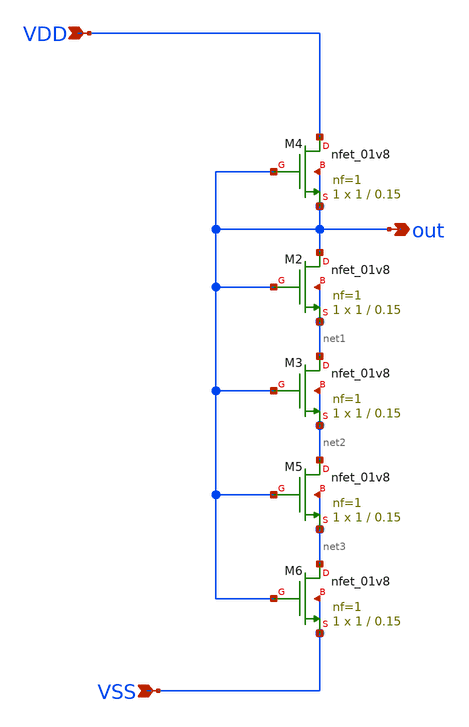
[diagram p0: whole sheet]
** sch_path: design/RPLY_TEMP_SENS_SKY130NM/RPLY_TEMP_SENS.sch
**.subckt RPLY_TEMP_SENS VDD VSS out
*.ipin VDD
*.ipin VSS
*.opin out
XM2 out out net1 net1 sky130_fd_pr__nfet_01v8 L=0.15 W=1 nf=1 ad='int((nf+1)/2) * W/nf * 0.29' as='int((nf+2)/2) * W/nf * 0.29'
+ pd='2*int((nf+1)/2) * (W/nf + 0.29)' ps='2*int((nf+2)/2) * (W/nf + 0.29)' nrd='0.29 / W' nrs='0.29 / W'
+ sa=0 sb=0 sd=0 mult=1 m=1
XM3 net1 out net2 net2 sky130_fd_pr__nfet_01v8 L=0.15 W=1 nf=1 ad='int((nf+1)/2) * W/nf * 0.29' as='int((nf+2)/2) * W/nf * 0.29'
+ pd='2*int((nf+1)/2) * (W/nf + 0.29)' ps='2*int((nf+2)/2) * (W/nf + 0.29)' nrd='0.29 / W' nrs='0.29 / W'
+ sa=0 sb=0 sd=0 mult=1 m=1
XM4 VDD out out out sky130_fd_pr__nfet_01v8 L=0.15 W=1 nf=1 ad='int((nf+1)/2) * W/nf * 0.29' as='int((nf+2)/2) * W/nf * 0.29'
+ pd='2*int((nf+1)/2) * (W/nf + 0.29)' ps='2*int((nf+2)/2) * (W/nf + 0.29)' nrd='0.29 / W' nrs='0.29 / W'
+ sa=0 sb=0 sd=0 mult=1 m=1
XM5 net2 out net3 net3 sky130_fd_pr__nfet_01v8 L=0.15 W=1 nf=1 ad='int((nf+1)/2) * W/nf * 0.29' as='int((nf+2)/2) * W/nf * 0.29'
+ pd='2*int((nf+1)/2) * (W/nf + 0.29)' ps='2*int((nf+2)/2) * (W/nf + 0.29)' nrd='0.29 / W' nrs='0.29 / W'
+ sa=0 sb=0 sd=0 mult=1 m=1
XM6 net3 out VSS VSS sky130_fd_pr__nfet_01v8 L=0.15 W=1 nf=1 ad='int((nf+1)/2) * W/nf * 0.29' as='int((nf+2)/2) * W/nf * 0.29'
+ pd='2*int((nf+1)/2) * (W/nf + 0.29)' ps='2*int((nf+2)/2) * (W/nf + 0.29)' nrd='0.29 / W' nrs='0.29 / W'
+ sa=0 sb=0 sd=0 mult=1 m=1
**.ends
.end
